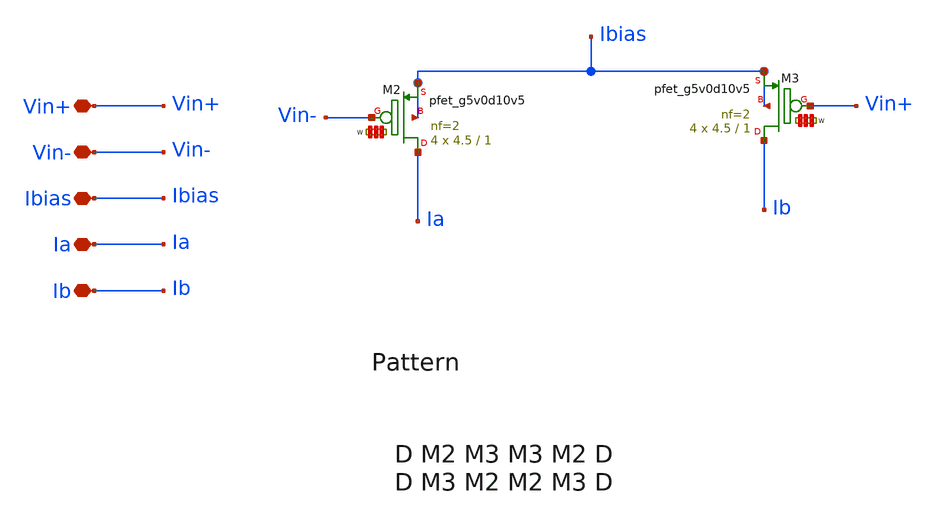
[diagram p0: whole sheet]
** sch_path: Learning/single_ended_amplifiers/VA001_series/Design_and_Analysis_of_Two-Stage_CMOS_Operational_Amplifier_for_Fluorescence_Signal_Processing_sky130_5V/amplifier_design/dif_pair.sch
**.subckt dif_pair Vin+ Vin- Ibias Ia Ib
*.iopin Vin+
*.iopin Vin-
*.iopin Ibias
*.iopin Ia
*.iopin Ib
XM2 Ia Vin- Ibias Ibias sky130_fd_pr__pfet_g5v0d10v5 L=1 W='4.5 * 2 ' nf=2 ad='int((2 + 1)/2) * 4.5 * 0.29'
+ as='int((2 + 2)/2) * 4.5 * 0.29' pd='2*int((2 + 1)/2) * (4.5 + 0.29)' ps='2*int((2 + 2)/2) * (4.5 + 0.29)'
+ nrd='0.29 / 4.5 / 2 ' nrs='0.29 / 4.5 / 2 ' sa=0 sb=0 sd=0 mult=4 m=4
XM3 Ib Vin+ Ibias Ibias sky130_fd_pr__pfet_g5v0d10v5 L=1 W='4.5 * 2 ' nf=2 ad='int((2 + 1)/2) * 4.5 * 0.29'
+ as='int((2 + 2)/2) * 4.5 * 0.29' pd='2*int((2 + 1)/2) * (4.5 + 0.29)' ps='2*int((2 + 2)/2) * (4.5 + 0.29)'
+ nrd='0.29 / 4.5 / 2 ' nrs='0.29 / 4.5 / 2 ' sa=0 sb=0 sd=0 mult=4 m=4
**.ends
.end
